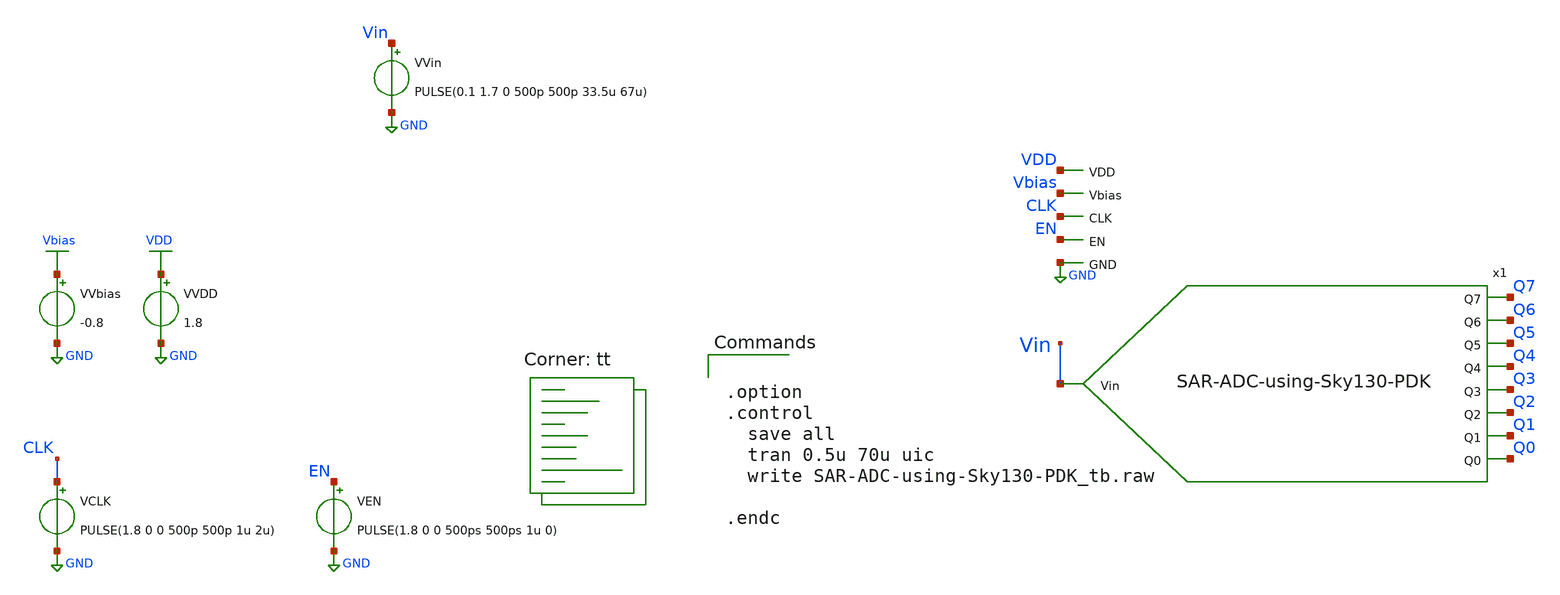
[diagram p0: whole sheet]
** sch_path: xschem/SAR-ADC-using-Sky130-PDK_tb.sch
**.subckt SAR-ADC-using-Sky130-PDK_tb
x1 VDD Vin Q0 Vbias EN Q1 CLK Q2 Q3 Q4 Q5 Q6 Q7 GND SAR-ADC-using-Sky130-PDK
VCLK CLK GND PULSE(1.8 0 0 500p 500p 1u 2u)
VVDD VDD GND 1.8
VEN EN GND PULSE(1.8 0 0 500ps 500ps 1u 0)
VVbias Vbias GND -0.8
VVin Vin GND PULSE(0.1 1.7 0 500p 500p 33.5u 67u)
**** begin user architecture code


.option
.control
  save all
  tran 0.5u 70u uic
  write SAR-ADC-using-Sky130-PDK_tb.raw

.endc


.lib $::SKYWATER_MODELS/sky130.lib.spice tt
**** end user architecture code
**.ends
.GLOBAL GND
.GLOBAL VDD
.GLOBAL Vbias
.end
